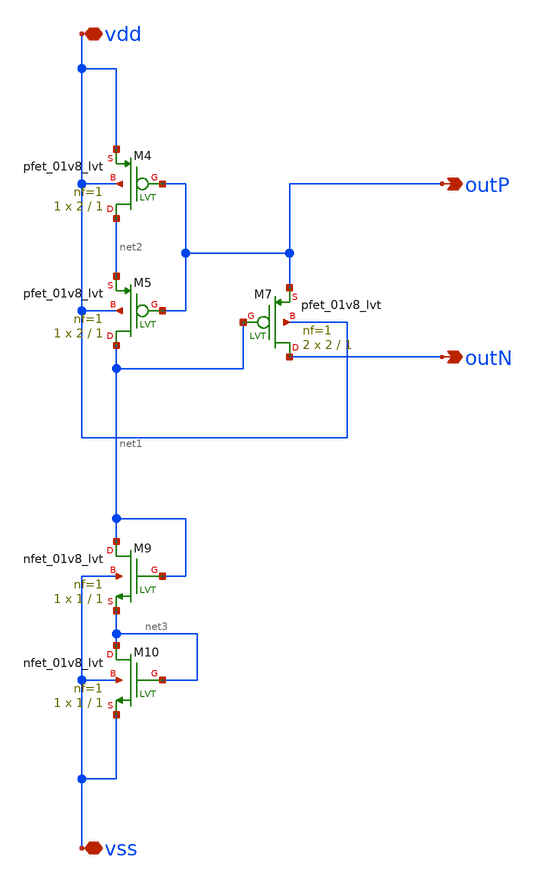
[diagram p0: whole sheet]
** sch_path: BGR_TOP_SKY130A/StartupCircuit.sch
**.subckt StartupCircuit vdd vss outP outN
*.iopin vdd
*.iopin vss
*.opin outP
*.opin outN
XM4 net2 outP vdd vdd sky130_fd_pr__pfet_01v8_lvt L=1 W=2 nf=1 ad='int((1 + 1)/2) * 2 / 1 * 0.29' as='int((1 + 2)/2) * 2 / 1 * 0.29'
+ pd='2*int((1 + 1)/2) * (2 / 1 + 0.29)' ps='2*int((1 + 2)/2) * (2 / 1 + 0.29)' nrd='0.29 / 2 ' nrs='0.29 / 2 '
+ sa=0 sb=0 sd=0 mult=1 m=1
XM7 outN net1 outP vdd sky130_fd_pr__pfet_01v8_lvt L=1 W=2 nf=1 ad='int((1 + 1)/2) * 2 / 1 * 0.29' as='int((1 + 2)/2) * 2 / 1 * 0.29'
+ pd='2*int((1 + 1)/2) * (2 / 1 + 0.29)' ps='2*int((1 + 2)/2) * (2 / 1 + 0.29)' nrd='0.29 / 2 ' nrs='0.29 / 2 '
+ sa=0 sb=0 sd=0 mult=2 m=2
XM9 net1 net1 net3 vss sky130_fd_pr__nfet_01v8_lvt L=1 W=1 nf=1 ad='int((1 + 1)/2) * 1 / 1 * 0.29' as='int((1 + 2)/2) * 1 / 1 * 0.29'
+ pd='2*int((1 + 1)/2) * (1 / 1 + 0.29)' ps='2*int((1 + 2)/2) * (1 / 1 + 0.29)' nrd='0.29 / 1 ' nrs='0.29 / 1 '
+ sa=0 sb=0 sd=0 mult=1 m=1
XM5 net1 outP net2 vdd sky130_fd_pr__pfet_01v8_lvt L=1 W=2 nf=1 ad='int((1 + 1)/2) * 2 / 1 * 0.29' as='int((1 + 2)/2) * 2 / 1 * 0.29'
+ pd='2*int((1 + 1)/2) * (2 / 1 + 0.29)' ps='2*int((1 + 2)/2) * (2 / 1 + 0.29)' nrd='0.29 / 2 ' nrs='0.29 / 2 '
+ sa=0 sb=0 sd=0 mult=1 m=1
XM10 net3 net3 vss vss sky130_fd_pr__nfet_01v8_lvt L=1 W=1 nf=1 ad='int((1 + 1)/2) * 1 / 1 * 0.29' as='int((1 + 2)/2) * 1 / 1 * 0.29'
+ pd='2*int((1 + 1)/2) * (1 / 1 + 0.29)' ps='2*int((1 + 2)/2) * (1 / 1 + 0.29)' nrd='0.29 / 1 ' nrs='0.29 / 1 '
+ sa=0 sb=0 sd=0 mult=1 m=1
**.ends
.end
